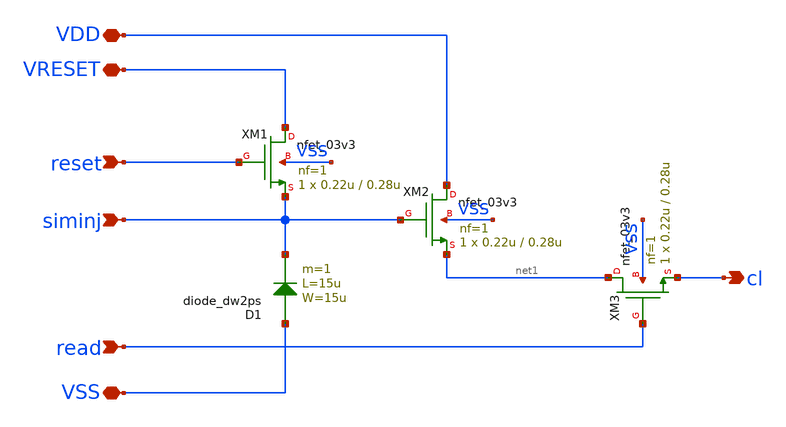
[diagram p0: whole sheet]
** sch_path: xschem/ip_pixel.sch
**.subckt ip_pixel VDD VSS siminj reset read VRESET cl
*.iopin VDD
*.iopin VSS
*.ipin siminj
*.ipin reset
*.ipin read
*.iopin VRESET
*.opin cl
D1 VSS siminj diode_dw2ps area='15u * 15u ' pj='2*15u + 2*15u ' m=1
XM1 VRESET reset siminj VSS nfet_03v3 L=0.28u W=0.22u nf=1 ad='int((nf+1)/2) * W/nf * 0.18u' as='int((nf+2)/2) * W/nf * 0.18u'
+ pd='2*int((nf+1)/2) * (W/nf + 0.18u)' ps='2*int((nf+2)/2) * (W/nf + 0.18u)' nrd='0.18u / W' nrs='0.18u / W'
+ sa=0 sb=0 sd=0 m=1
XM2 VDD siminj net1 VSS nfet_03v3 L=0.28u W=0.22u nf=1 ad='int((nf+1)/2) * W/nf * 0.18u' as='int((nf+2)/2) * W/nf * 0.18u'
+ pd='2*int((nf+1)/2) * (W/nf + 0.18u)' ps='2*int((nf+2)/2) * (W/nf + 0.18u)' nrd='0.18u / W' nrs='0.18u / W'
+ sa=0 sb=0 sd=0 m=1
XM3 net1 read cl VSS nfet_03v3 L=0.28u W=0.22u nf=1 ad='int((nf+1)/2) * W/nf * 0.18u' as='int((nf+2)/2) * W/nf * 0.18u'
+ pd='2*int((nf+1)/2) * (W/nf + 0.18u)' ps='2*int((nf+2)/2) * (W/nf + 0.18u)' nrd='0.18u / W' nrs='0.18u / W'
+ sa=0 sb=0 sd=0 m=1
**.ends
.end
